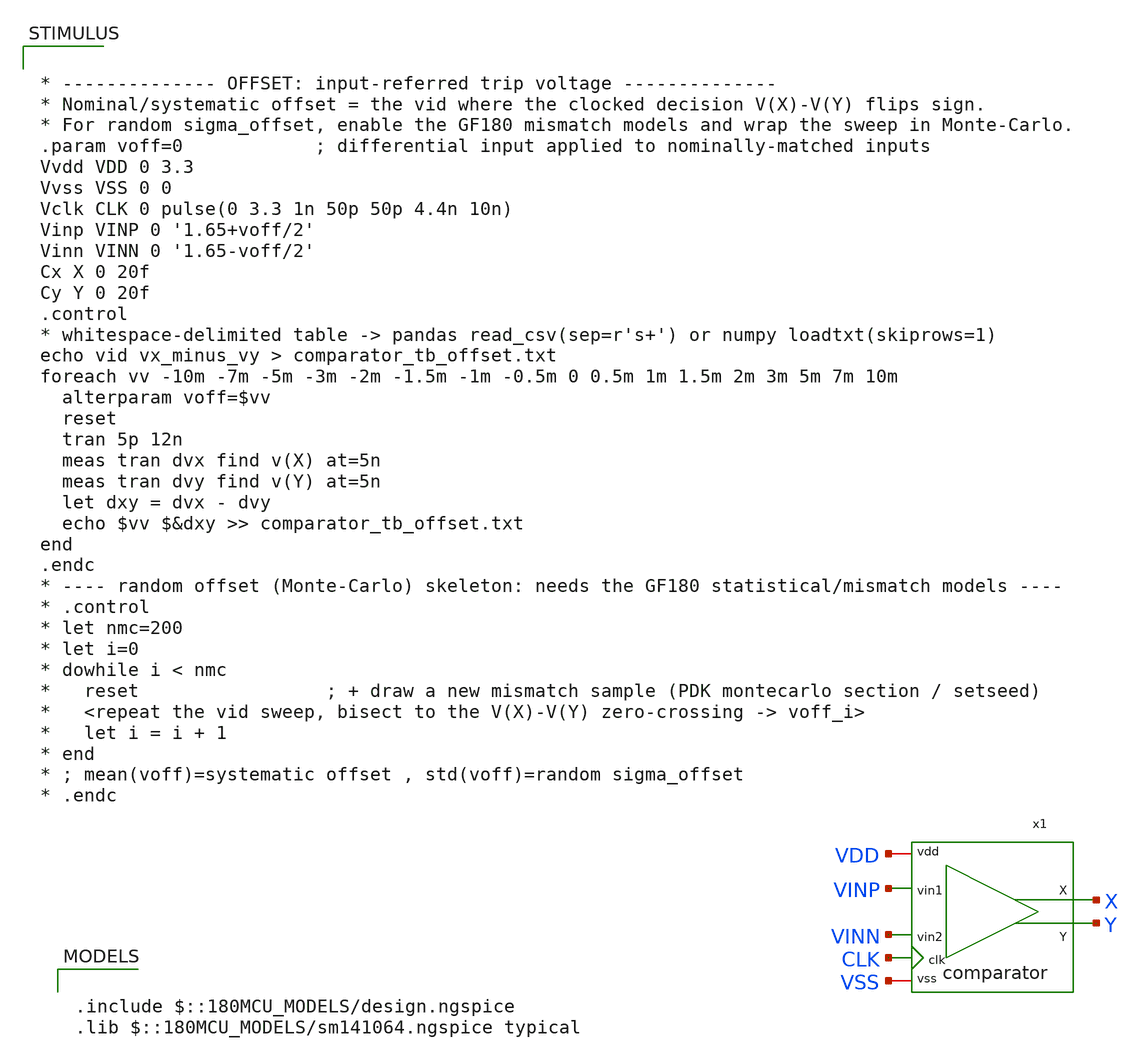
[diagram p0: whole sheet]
** sch_path: designs/libs/core_analog/saradc/tb/comparator_tb_offset.sch
**.subckt comparator_tb_offset
x1 VDD VSS X VINP Y VINN CLK comparator
**** begin user architecture code

.include $::180MCU_MODELS/design.ngspice
.lib $::180MCU_MODELS/sm141064.ngspice typical



* -------------- OFFSET: input-referred trip voltage --------------
* Nominal/systematic offset = the vid where the clocked decision V(X)-V(Y) flips sign.
* For random sigma_offset, enable the GF180 mismatch models and wrap the sweep in Monte-Carlo.
.param voff=0            ; differential input applied to nominally-matched inputs
Vvdd VDD 0 3.3
Vvss VSS 0 0
Vclk CLK 0 pulse(0 3.3 1n 50p 50p 4.4n 10n)
Vinp VINP 0 '1.65+voff/2'
Vinn VINN 0 '1.65-voff/2'
Cx X 0 20f
Cy Y 0 20f
.control
* whitespace-delimited table -> pandas read_csv(sep=r's+') or numpy loadtxt(skiprows=1)
echo vid vx_minus_vy > comparator_tb_offset.txt
foreach vv -10m -7m -5m -3m -2m -1.5m -1m -0.5m 0 0.5m 1m 1.5m 2m 3m 5m 7m 10m
  alterparam voff=$vv
  reset
  tran 5p 12n
  meas tran dvx find v(X) at=5n
  meas tran dvy find v(Y) at=5n
  let dxy = dvx - dvy
  echo $vv $&dxy >> comparator_tb_offset.txt
end
.endc
* ---- random offset (Monte-Carlo) skeleton: needs the GF180 statistical/mismatch models ----
* .control
* let nmc=200
* let i=0
* dowhile i < nmc
*   reset                 ; + draw a new mismatch sample (PDK montecarlo section / setseed)
*   <repeat the vid sweep, bisect to the V(X)-V(Y) zero-crossing -> voff_i>
*   let i = i + 1
* end
* ; mean(voff)=systematic offset , std(voff)=random sigma_offset
* .endc


**** end user architecture code
**.ends

* expanding   symbol:  comparator.sym # of pins=7
** sym_path: designs/libs/core_analog/saradc/comparator.sym
** sch_path: designs/libs/core_analog/saradc/comparator.sch
.subckt comparator vdd vss X vin1 Y vin2 clk
*.iopin vdd
*.iopin vss
*.ipin vin1
*.ipin vin2
*.ipin clk
*.opin X
*.opin Y
XM1 P vin1 net1 vss nfet_03v3 L=0.5u W=4u nf=4 ad='int((nf+1)/2) * W/nf * 0.18u' as='int((nf+2)/2) * W/nf * 0.18u'
+ pd='2*int((nf+1)/2) * (W/nf + 0.18u)' ps='2*int((nf+2)/2) * (W/nf + 0.18u)' nrd='0.18u / W' nrs='0.18u / W'
+ sa=0 sb=0 sd=0 m=1
XM2 Q vin2 net1 vss nfet_03v3 L=0.5u W=4u nf=4 ad='int((nf+1)/2) * W/nf * 0.18u' as='int((nf+2)/2) * W/nf * 0.18u'
+ pd='2*int((nf+1)/2) * (W/nf + 0.18u)' ps='2*int((nf+2)/2) * (W/nf + 0.18u)' nrd='0.18u / W' nrs='0.18u / W'
+ sa=0 sb=0 sd=0 m=1
XM3 X Y P vss nfet_03v3 L=0.28u W=2u nf=2 ad='int((nf+1)/2) * W/nf * 0.18u' as='int((nf+2)/2) * W/nf * 0.18u'
+ pd='2*int((nf+1)/2) * (W/nf + 0.18u)' ps='2*int((nf+2)/2) * (W/nf + 0.18u)' nrd='0.18u / W' nrs='0.18u / W'
+ sa=0 sb=0 sd=0 m=1
XM4 Y X Q vss nfet_03v3 L=0.28u W=2u nf=2 ad='int((nf+1)/2) * W/nf * 0.18u' as='int((nf+2)/2) * W/nf * 0.18u'
+ pd='2*int((nf+1)/2) * (W/nf + 0.18u)' ps='2*int((nf+2)/2) * (W/nf + 0.18u)' nrd='0.18u / W' nrs='0.18u / W'
+ sa=0 sb=0 sd=0 m=1
XM5 X Y vdd vdd pfet_03v3 L=0.28u W=6u nf=2 ad='int((nf+1)/2) * W/nf * 0.18u' as='int((nf+2)/2) * W/nf * 0.18u'
+ pd='2*int((nf+1)/2) * (W/nf + 0.18u)' ps='2*int((nf+2)/2) * (W/nf + 0.18u)' nrd='0.18u / W' nrs='0.18u / W'
+ sa=0 sb=0 sd=0 m=1
XM6 Y X vdd vdd pfet_03v3 L=0.28u W=6u nf=2 ad='int((nf+1)/2) * W/nf * 0.18u' as='int((nf+2)/2) * W/nf * 0.18u'
+ pd='2*int((nf+1)/2) * (W/nf + 0.18u)' ps='2*int((nf+2)/2) * (W/nf + 0.18u)' nrd='0.18u / W' nrs='0.18u / W'
+ sa=0 sb=0 sd=0 m=1
XM7 net1 clk vss vss nfet_03v3 L=0.28u W=6u nf=4 ad='int((nf+1)/2) * W/nf * 0.18u' as='int((nf+2)/2) * W/nf * 0.18u'
+ pd='2*int((nf+1)/2) * (W/nf + 0.18u)' ps='2*int((nf+2)/2) * (W/nf + 0.18u)' nrd='0.18u / W' nrs='0.18u / W'
+ sa=0 sb=0 sd=0 m=1
XM8 X clk vdd vdd pfet_03v3 L=0.28u W=2u nf=1 ad='int((nf+1)/2) * W/nf * 0.18u' as='int((nf+2)/2) * W/nf * 0.18u'
+ pd='2*int((nf+1)/2) * (W/nf + 0.18u)' ps='2*int((nf+2)/2) * (W/nf + 0.18u)' nrd='0.18u / W' nrs='0.18u / W'
+ sa=0 sb=0 sd=0 m=1
XM9 P clk vdd vdd pfet_03v3 L=0.28u W=2u nf=1 ad='int((nf+1)/2) * W/nf * 0.18u' as='int((nf+2)/2) * W/nf * 0.18u'
+ pd='2*int((nf+1)/2) * (W/nf + 0.18u)' ps='2*int((nf+2)/2) * (W/nf + 0.18u)' nrd='0.18u / W' nrs='0.18u / W'
+ sa=0 sb=0 sd=0 m=1
XM10 Y clk vdd vdd pfet_03v3 L=0.28u W=2u nf=1 ad='int((nf+1)/2) * W/nf * 0.18u' as='int((nf+2)/2) * W/nf * 0.18u'
+ pd='2*int((nf+1)/2) * (W/nf + 0.18u)' ps='2*int((nf+2)/2) * (W/nf + 0.18u)' nrd='0.18u / W' nrs='0.18u / W'
+ sa=0 sb=0 sd=0 m=1
XM11 Q clk vdd vdd pfet_03v3 L=0.28u W=2u nf=1 ad='int((nf+1)/2) * W/nf * 0.18u' as='int((nf+2)/2) * W/nf * 0.18u'
+ pd='2*int((nf+1)/2) * (W/nf + 0.18u)' ps='2*int((nf+2)/2) * (W/nf + 0.18u)' nrd='0.18u / W' nrs='0.18u / W'
+ sa=0 sb=0 sd=0 m=1
.ends

.end
